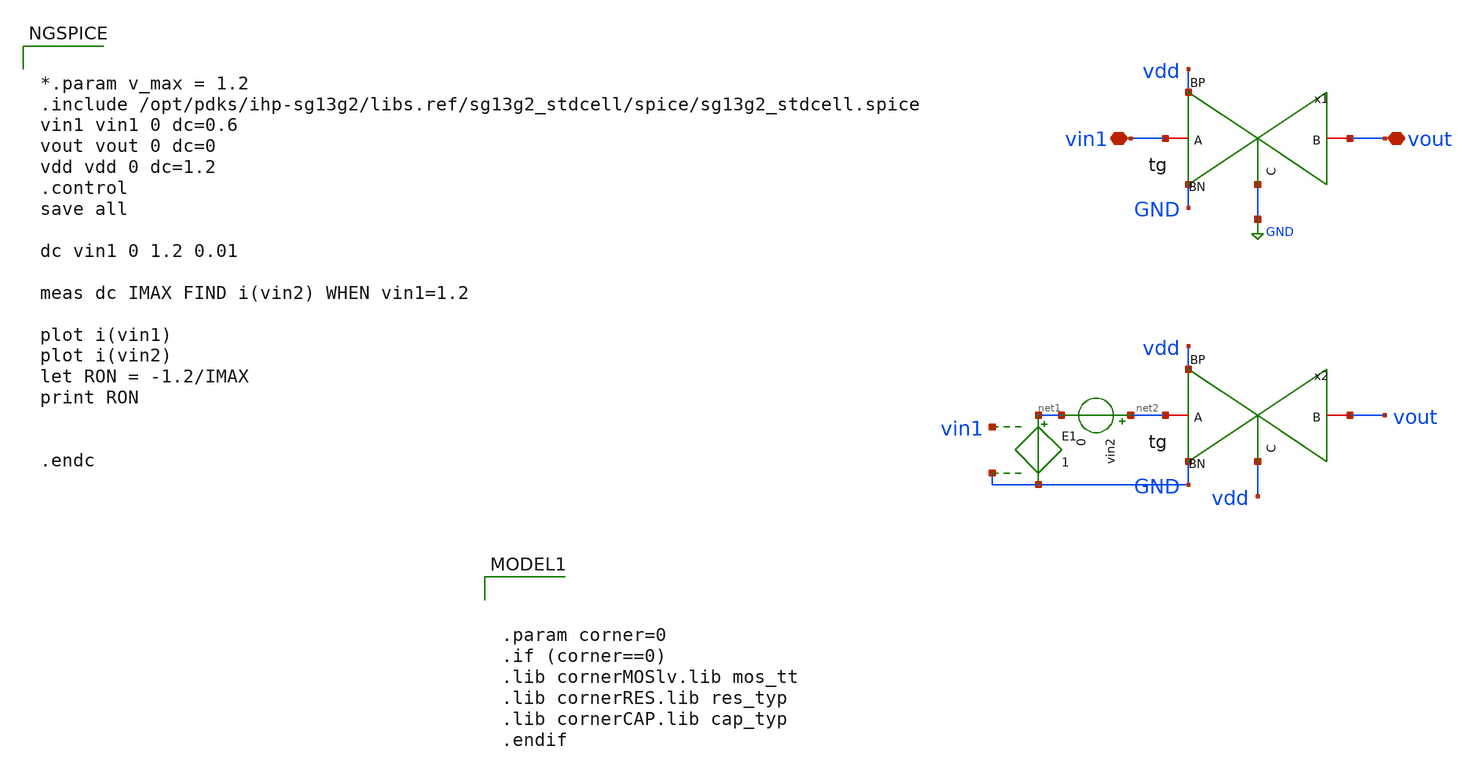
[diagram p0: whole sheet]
** sch_path: src/analog/tg/tb_tg.sch
**.subckt tb_tg vin1 vout
*.iopin vin1
*.iopin vout
x1 vout GND vin1 vdd GND tg
x2 vout vdd net2 vdd GND tg
E1 net1 GND vin1 GND 1
vin2 net2 net1 0
**** begin user architecture code


*.param v_max = 1.2
.include /opt/pdks/ihp-sg13g2/libs.ref/sg13g2_stdcell/spice/sg13g2_stdcell.spice
vin1 vin1 0 dc=0.6
vout vout 0 dc=0
vdd vdd 0 dc=1.2
.control
save all

dc vin1 0 1.2 0.01

meas dc IMAX FIND i(vin2) WHEN vin1=1.2

plot i(vin1)
plot i(vin2)
let RON = -1.2/IMAX
print RON


.endc




.param corner=0
.if (corner==0)
.lib cornerMOSlv.lib mos_tt
.lib cornerRES.lib res_typ
.lib cornerCAP.lib cap_typ
.endif

**** end user architecture code
**.ends

* expanding   symbol:  /home/designer/shared/ihp-sg13g2_ana_mux_32_1_serial_sel/src/analog/tg/tg.sym
*+ # of pins=5
** sym_path: src/analog/tg/tg.sym
** sch_path: src/analog/tg/tg.sch
.subckt tg B C A BP BN
*.iopin B
*.iopin A
*.iopin BN
*.iopin BP
*.iopin C
XM1 A C B BN sg13_lv_nmos w=120u l=0.13u ng=200 m=1 mm_ok=1
XM2 A net1 B BP sg13_lv_pmos w=300u l=0.13u ng=200 m=1 mm_ok=1
x1 net1 C BP BN sg13g2_inv_1
.ends


* expanding   symbol:  sg13g2_stdcells/sg13g2_inv_1.sym # of pins=2
** sym_path: sg13g2_stdcells/sg13g2_inv_1.sym
** sch_path: sg13g2_stdcells/sg13g2_inv_1.sch
.subckt sg13g2_inv_1 Y A VDD VSS
*.opin Y
*.ipin A
*.iopin VDD
*.iopin VSS
XM1 Y A VSS VSS sg13_lv_nmos w=740.00n l=130.00n ng=1 m=1 mm_ok=1
XM2 Y A VDD VDD sg13_lv_pmos w=1.12u l=130.00n ng=1 m=1 mm_ok=1
.ends

.GLOBAL GND
.end
